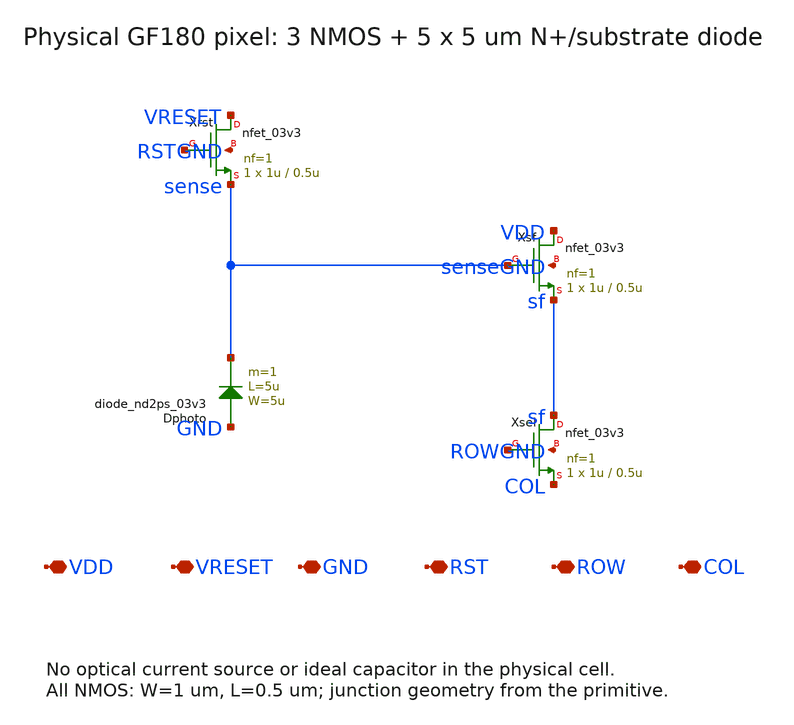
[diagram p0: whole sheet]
** sch_path: xschem/pixel_physical.sch
**.subckt pixel_physical VDD VRESET GND RST ROW COL
*.iopin VDD
*.iopin VRESET
*.iopin GND
*.iopin RST
*.iopin ROW
*.iopin COL
Xrst VRESET RST sense GND nfet_03v3 L=0.5u W=1u nf=1 ad=0.44p as=0.44p pd=2.88u ps=2.88u nrd=0 nrs=0
+ sa=0 sb=0 sd=0 m=1
Xsf VDD sense sf GND nfet_03v3 L=0.5u W=1u nf=1 ad=0.44p as=0.44p pd=2.88u ps=2.88u nrd=0 nrs=0 sa=0
+ sb=0 sd=0 m=1
Xsel sf ROW COL GND nfet_03v3 L=0.5u W=1u nf=1 ad=0.44p as=0.44p pd=2.88u ps=2.88u nrd=0 nrs=0 sa=0
+ sb=0 sd=0 m=1
Dphoto GND sense diode_nd2ps_03v3 area='5u * 5u ' pj='2*5u + 2*5u ' m=1
**.ends
.end
